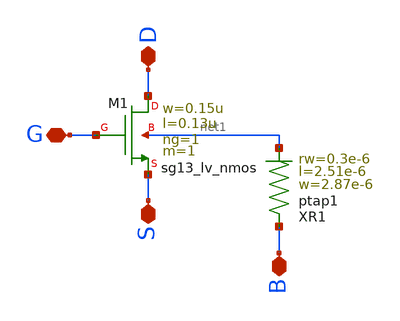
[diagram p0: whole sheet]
** sch_path: LVS-testbenches/schematic/sg13_lv_nmos_ring.sch
**.subckt sg13_lv_nmos_ring D S G B
*.iopin D
*.iopin S
*.iopin G
*.iopin B
XM1 D G S net1 sg13_lv_nmos w=0.15u l=0.13u ng=1 m=1 mm_ok=1
XR1 B net1 ptap1 R=23.84 w=2.87e-6 l=2.51e-6 rw=0.3e-6
**.ends
.end
